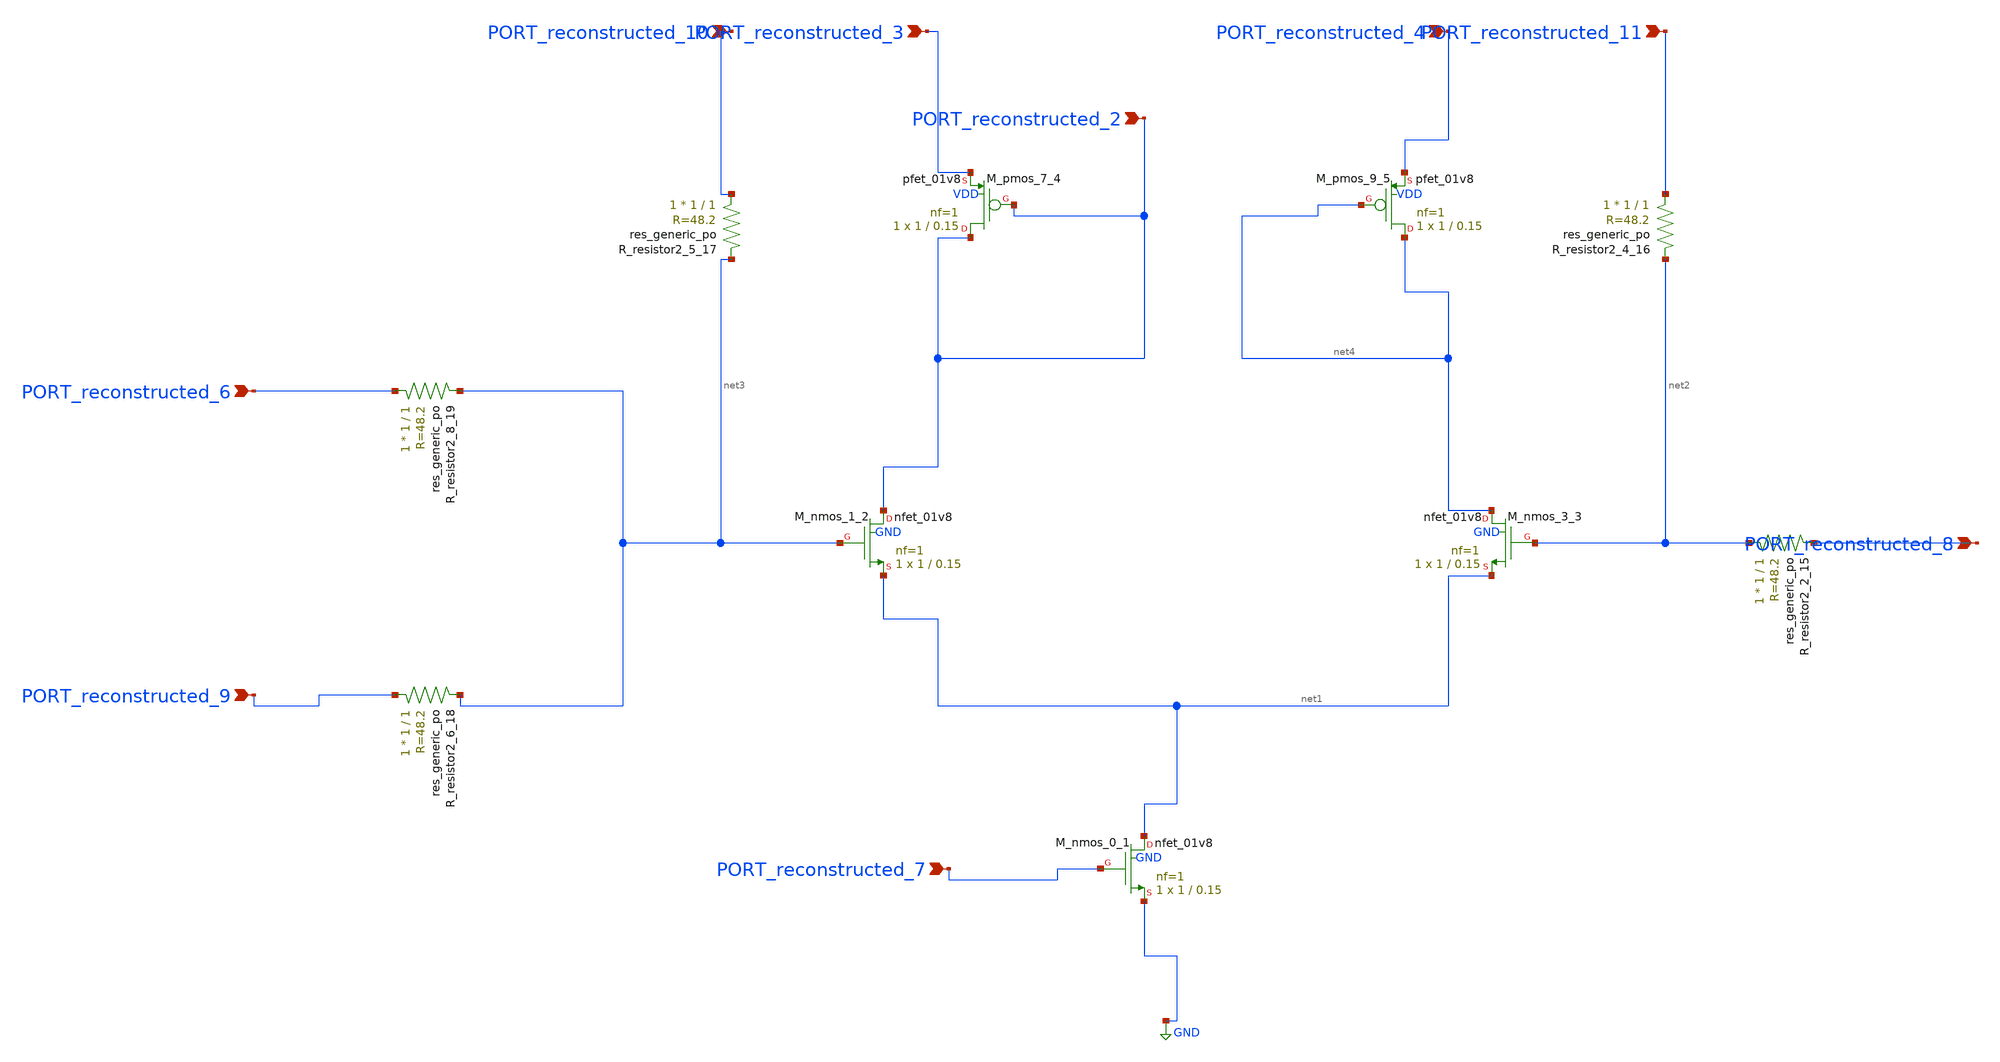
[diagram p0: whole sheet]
** sch_path: schematics/SchemGen/p05_fig8_cmfb.sch
**.subckt p05_fig8_cmfb PORT_reconstructed_6 PORT_reconstructed_2 PORT_reconstructed_7
*+ PORT_reconstructed_8 PORT_reconstructed_9 PORT_reconstructed_10 PORT_reconstructed_11 PORT_reconstructed_4
*+ PORT_reconstructed_3
*.ipin PORT_reconstructed_6
*.ipin PORT_reconstructed_2
*.ipin PORT_reconstructed_7
*.ipin PORT_reconstructed_8
*.ipin PORT_reconstructed_9
*.ipin PORT_reconstructed_10
*.ipin PORT_reconstructed_11
*.ipin PORT_reconstructed_4
*.ipin PORT_reconstructed_3
XM_nmos_0_1 net1 PORT_reconstructed_7 GND GND sky130_fd_pr__nfet_01v8 L=0.15 W=1 nf=1 ad='int((1 + 1)/2) * 1 / 1 * 0.29'
+ as='int((1 + 2)/2) * 1 / 1 * 0.29' pd='2*int((1 + 1)/2) * (1 / 1 + 0.29)' ps='2*int((1 + 2)/2) * (1 / 1 + 0.29)'
+ nrd='0.29 / 1 ' nrs='0.29 / 1 ' sa=0 sb=0 sd=0 mult=1 m=1
XM_nmos_1_2 PORT_reconstructed_2 net3 net1 GND sky130_fd_pr__nfet_01v8 L=0.15 W=1 nf=1 ad='int((1 + 1)/2) * 1 / 1 * 0.29'
+ as='int((1 + 2)/2) * 1 / 1 * 0.29' pd='2*int((1 + 1)/2) * (1 / 1 + 0.29)' ps='2*int((1 + 2)/2) * (1 / 1 + 0.29)'
+ nrd='0.29 / 1 ' nrs='0.29 / 1 ' sa=0 sb=0 sd=0 mult=1 m=1
XM_nmos_3_3 net4 net2 net1 GND sky130_fd_pr__nfet_01v8 L=0.15 W=1 nf=1 ad='int((1 + 1)/2) * 1 / 1 * 0.29'
+ as='int((1 + 2)/2) * 1 / 1 * 0.29' pd='2*int((1 + 1)/2) * (1 / 1 + 0.29)' ps='2*int((1 + 2)/2) * (1 / 1 + 0.29)'
+ nrd='0.29 / 1 ' nrs='0.29 / 1 ' sa=0 sb=0 sd=0 mult=1 m=1
XM_pmos_7_4 PORT_reconstructed_2 PORT_reconstructed_2 PORT_reconstructed_3 VDD sky130_fd_pr__pfet_01v8
+ L=0.15 W=1 nf=1 ad='int((1 + 1)/2) * 1 / 1 * 0.29' as='int((1 + 2)/2) * 1 / 1 * 0.29' pd='2*int((1 + 1)/2) * (1 / 1 + 0.29)'
+ ps='2*int((1 + 2)/2) * (1 / 1 + 0.29)' nrd='0.29 / 1 ' nrs='0.29 / 1 ' sa=0 sb=0 sd=0 mult=1 m=1
XM_pmos_9_5 net4 net4 PORT_reconstructed_4 VDD sky130_fd_pr__pfet_01v8 L=0.15 W=1 nf=1 ad='int((1 + 1)/2) * 1 / 1 * 0.29'
+ as='int((1 + 2)/2) * 1 / 1 * 0.29' pd='2*int((1 + 1)/2) * (1 / 1 + 0.29)' ps='2*int((1 + 2)/2) * (1 / 1 + 0.29)'
+ nrd='0.29 / 1 ' nrs='0.29 / 1 ' sa=0 sb=0 sd=0 mult=1 m=1
XR_resistor2_2_15 net2 PORT_reconstructed_8 sky130_fd_pr__res_generic_po W=1 L=1 m=1
XR_resistor2_4_16 PORT_reconstructed_11 net2 sky130_fd_pr__res_generic_po W=1 L=1 m=1
XR_resistor2_5_17 PORT_reconstructed_10 net3 sky130_fd_pr__res_generic_po W=1 L=1 m=1
XR_resistor2_6_18 PORT_reconstructed_9 net3 sky130_fd_pr__res_generic_po W=1 L=1 m=1
XR_resistor2_8_19 PORT_reconstructed_6 net3 sky130_fd_pr__res_generic_po W=1 L=1 m=1
**.ends
.GLOBAL GND
.end
